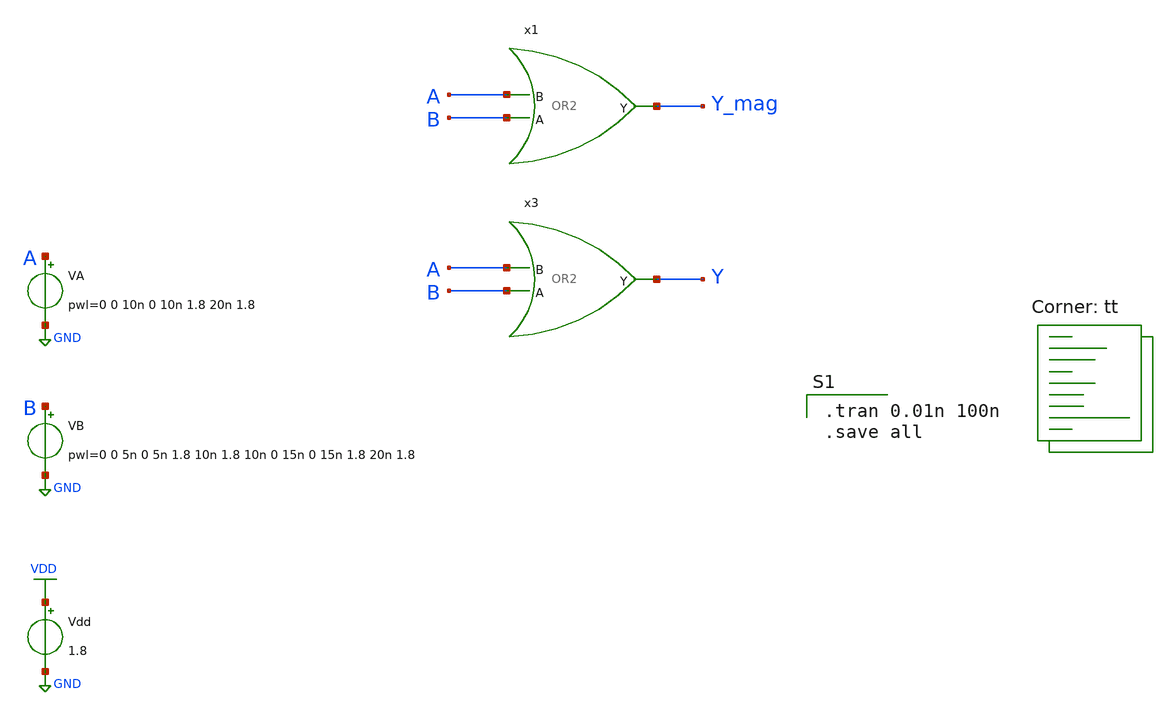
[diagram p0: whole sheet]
** sch_path: OR2sim.sch
**.subckt OR2sim
Vdd VDD GND 1.8
VA A GND pwl=0 0 10n 0 10n 1.8 20n 1.8
VB B GND pwl=0 0 5n 0 5n 1.8 10n 1.8 10n 0 15n 0 15n 1.8 20n 1.8
x3 A Y B OR2
x1 A Y_mag B OR2.parax
**** begin user architecture code

.tran 0.01n 100n
.save all

.lib $::SKYWATER_MODELS/sky130.lib.spice tt
**** end user architecture code
**.ends

* expanding   symbol:  gates/OR2.sym # of pins=3
** sym_path: gates/OR2.sym
** sch_path: gates/OR2.sch
.subckt OR2 B Y A
*.ipin A
*.ipin B
*.opin Y
XM7 VDD B net2 VDD sky130_fd_pr__pfet_01v8 L=0.15 W=1 nf=1 ad='int((nf+1)/2) * W/nf * 0.29' as='int((nf+2)/2) * W/nf * 0.29'
+ pd='2*int((nf+1)/2) * (W/nf + 0.29)' ps='2*int((nf+2)/2) * (W/nf + 0.29)' nrd='0.29 / W' nrs='0.29 / W'
+ sa=0 sb=0 sd=0 mult=1 m=1
XM8 GND B net1 GND sky130_fd_pr__nfet_01v8 L=0.15 W=1 nf=1 ad='int((nf+1)/2) * W/nf * 0.29' as='int((nf+2)/2) * W/nf * 0.29'
+ pd='2*int((nf+1)/2) * (W/nf + 0.29)' ps='2*int((nf+2)/2) * (W/nf + 0.29)' nrd='0.29 / W' nrs='0.29 / W'
+ sa=0 sb=0 sd=0 mult=1 m=1
XM9 net2 A net1 VDD sky130_fd_pr__pfet_01v8 L=0.15 W=1 nf=1 ad='int((nf+1)/2) * W/nf * 0.29' as='int((nf+2)/2) * W/nf * 0.29'
+ pd='2*int((nf+1)/2) * (W/nf + 0.29)' ps='2*int((nf+2)/2) * (W/nf + 0.29)' nrd='0.29 / W' nrs='0.29 / W'
+ sa=0 sb=0 sd=0 mult=1 m=1
XM10 GND A net1 GND sky130_fd_pr__nfet_01v8 L=0.15 W=1 nf=1 ad='int((nf+1)/2) * W/nf * 0.29' as='int((nf+2)/2) * W/nf * 0.29'
+ pd='2*int((nf+1)/2) * (W/nf + 0.29)' ps='2*int((nf+2)/2) * (W/nf + 0.29)' nrd='0.29 / W' nrs='0.29 / W'
+ sa=0 sb=0 sd=0 mult=1 m=1
X1 net1 Y inv_vtc
.ends


* expanding   symbol:  gates/OR2.parax.sym # of pins=3
** sym_path: gates/OR2.sym
.include [file normalize /home/apn/mag_gates/OR2.parax.spice]

* expanding   symbol:  /home/apn/test_xschem_sky130/inv_vtc.sym # of pins=2
** sym_path: inv_vtc.sym
** sch_path: inv_vtc.sch
.subckt inv_vtc A Y
*.ipin A
*.opin Y
XM1 Y A VDD VDD sky130_fd_pr__pfet_01v8 L=0.15 W=2 nf=1 ad='int((nf+1)/2) * W/nf * 0.29' as='int((nf+2)/2) * W/nf * 0.29'
+ pd='2*int((nf+1)/2) * (W/nf + 0.29)' ps='2*int((nf+2)/2) * (W/nf + 0.29)' nrd='0.29 / W' nrs='0.29 / W'
+ sa=0 sb=0 sd=0 mult=1 m=1
XM2 Y A GND GND sky130_fd_pr__nfet_01v8 L=0.15 W=1 nf=1 ad='int((nf+1)/2) * W/nf * 0.29' as='int((nf+2)/2) * W/nf * 0.29'
+ pd='2*int((nf+1)/2) * (W/nf + 0.29)' ps='2*int((nf+2)/2) * (W/nf + 0.29)' nrd='0.29 / W' nrs='0.29 / W'
+ sa=0 sb=0 sd=0 mult=1 m=1
.ends

.GLOBAL VDD
.GLOBAL GND
.end
